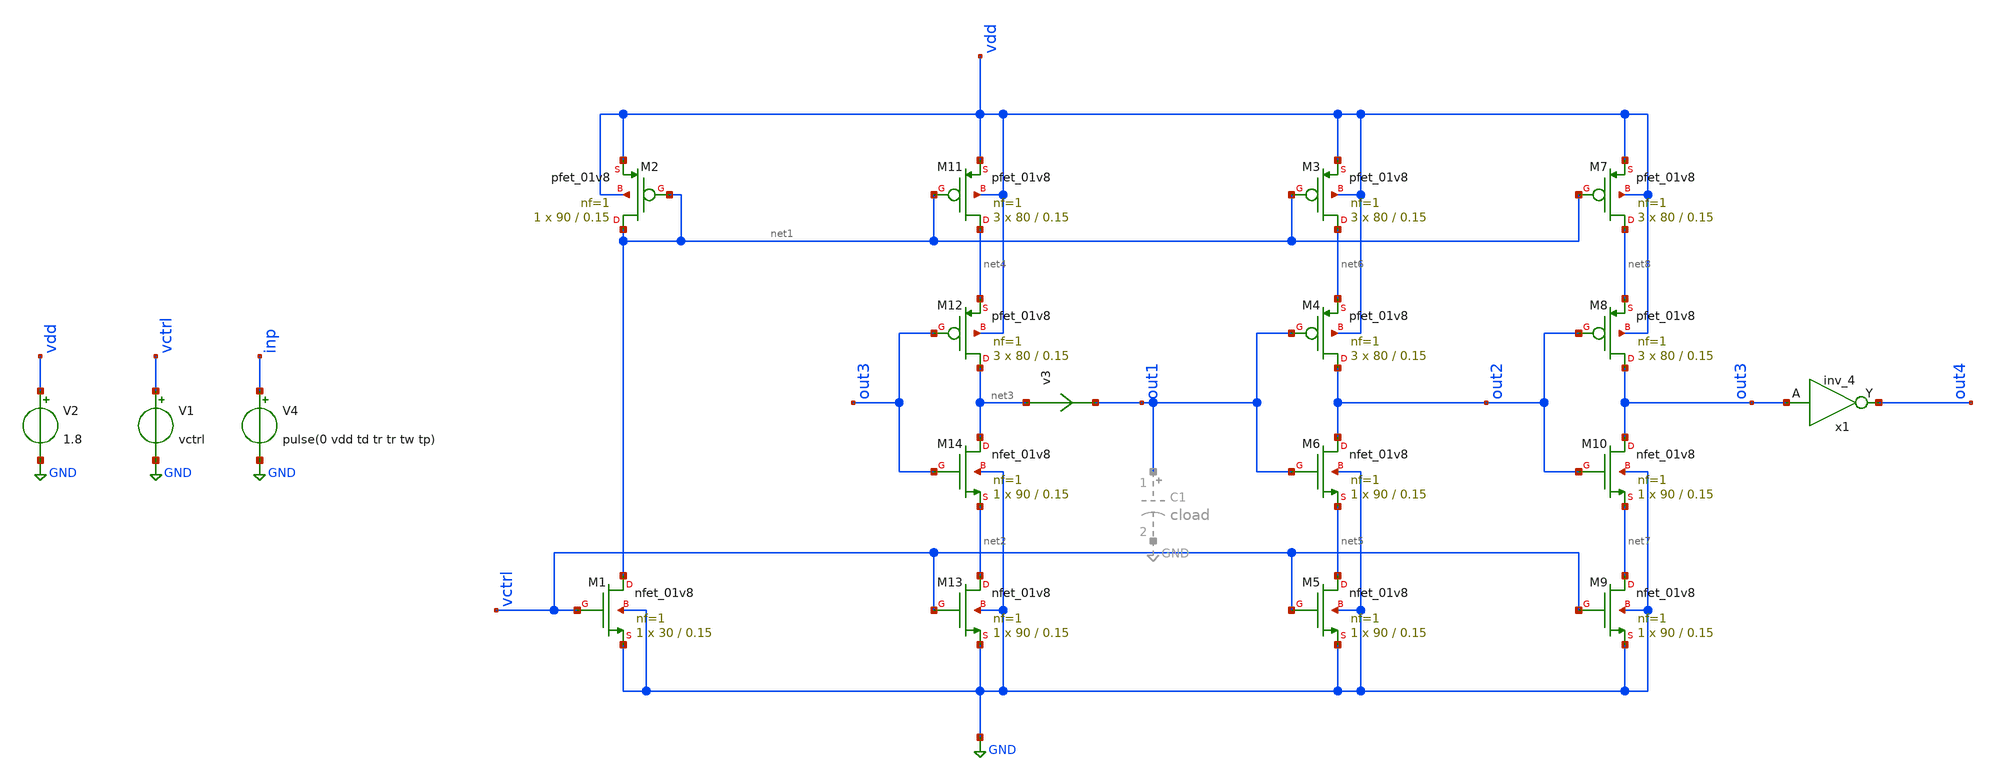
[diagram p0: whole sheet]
** sch_path: xschem/vco/inv_delay01_issue.sch
**.subckt inv_delay01_issue
XM1 net1 vctrl GND GND sky130_fd_pr__nfet_01v8 L=0.15 W=30 nf=1 ad='int((nf+1)/2) * W/nf * 0.29' as='int((nf+2)/2) * W/nf * 0.29'
+ pd='2*int((nf+1)/2) * (W/nf + 0.29)' ps='2*int((nf+2)/2) * (W/nf + 0.29)' nrd='0.29 / W' nrs='0.29 / W'
+ sa=0 sb=0 sd=0 mult=1 m=1
XM2 net1 net1 vdd vdd sky130_fd_pr__pfet_01v8 L=0.15 W=90 nf=1 ad='int((nf+1)/2) * W/nf * 0.29' as='int((nf+2)/2) * W/nf * 0.29'
+ pd='2*int((nf+1)/2) * (W/nf + 0.29)' ps='2*int((nf+2)/2) * (W/nf + 0.29)' nrd='0.29 / W' nrs='0.29 / W'
+ sa=0 sb=0 sd=0 mult=1 m=1
XM11 net4 net1 vdd vdd sky130_fd_pr__pfet_01v8 L=0.15 W=80 nf=1 ad='int((nf+1)/2) * W/nf * 0.29' as='int((nf+2)/2) * W/nf * 0.29'
+ pd='2*int((nf+1)/2) * (W/nf + 0.29)' ps='2*int((nf+2)/2) * (W/nf + 0.29)' nrd='0.29 / W' nrs='0.29 / W'
+ sa=0 sb=0 sd=0 mult=3 m=3
XM12 net3 out3 net4 vdd sky130_fd_pr__pfet_01v8 L=0.15 W=80 nf=1 ad='int((nf+1)/2) * W/nf * 0.29' as='int((nf+2)/2) * W/nf * 0.29'
+ pd='2*int((nf+1)/2) * (W/nf + 0.29)' ps='2*int((nf+2)/2) * (W/nf + 0.29)' nrd='0.29 / W' nrs='0.29 / W'
+ sa=0 sb=0 sd=0 mult=3 m=3
XM13 net2 vctrl GND GND sky130_fd_pr__nfet_01v8 L=0.15 W=90 nf=1 ad='int((nf+1)/2) * W/nf * 0.29' as='int((nf+2)/2) * W/nf * 0.29'
+ pd='2*int((nf+1)/2) * (W/nf + 0.29)' ps='2*int((nf+2)/2) * (W/nf + 0.29)' nrd='0.29 / W' nrs='0.29 / W'
+ sa=0 sb=0 sd=0 mult=1 m=1
XM14 net3 out3 net2 GND sky130_fd_pr__nfet_01v8 L=0.15 W=90 nf=1 ad='int((nf+1)/2) * W/nf * 0.29' as='int((nf+2)/2) * W/nf * 0.29'
+ pd='2*int((nf+1)/2) * (W/nf + 0.29)' ps='2*int((nf+2)/2) * (W/nf + 0.29)' nrd='0.29 / W' nrs='0.29 / W'
+ sa=0 sb=0 sd=0 mult=1 m=1
XM3 net6 net1 vdd vdd sky130_fd_pr__pfet_01v8 L=0.15 W=80 nf=1 ad='int((nf+1)/2) * W/nf * 0.29' as='int((nf+2)/2) * W/nf * 0.29'
+ pd='2*int((nf+1)/2) * (W/nf + 0.29)' ps='2*int((nf+2)/2) * (W/nf + 0.29)' nrd='0.29 / W' nrs='0.29 / W'
+ sa=0 sb=0 sd=0 mult=3 m=3
XM4 out2 out1 net6 vdd sky130_fd_pr__pfet_01v8 L=0.15 W=80 nf=1 ad='int((nf+1)/2) * W/nf * 0.29' as='int((nf+2)/2) * W/nf * 0.29'
+ pd='2*int((nf+1)/2) * (W/nf + 0.29)' ps='2*int((nf+2)/2) * (W/nf + 0.29)' nrd='0.29 / W' nrs='0.29 / W'
+ sa=0 sb=0 sd=0 mult=3 m=3
XM5 net5 vctrl GND GND sky130_fd_pr__nfet_01v8 L=0.15 W=90 nf=1 ad='int((nf+1)/2) * W/nf * 0.29' as='int((nf+2)/2) * W/nf * 0.29'
+ pd='2*int((nf+1)/2) * (W/nf + 0.29)' ps='2*int((nf+2)/2) * (W/nf + 0.29)' nrd='0.29 / W' nrs='0.29 / W'
+ sa=0 sb=0 sd=0 mult=1 m=1
XM6 out2 out1 net5 GND sky130_fd_pr__nfet_01v8 L=0.15 W=90 nf=1 ad='int((nf+1)/2) * W/nf * 0.29' as='int((nf+2)/2) * W/nf * 0.29'
+ pd='2*int((nf+1)/2) * (W/nf + 0.29)' ps='2*int((nf+2)/2) * (W/nf + 0.29)' nrd='0.29 / W' nrs='0.29 / W'
+ sa=0 sb=0 sd=0 mult=1 m=1
XM7 net8 net1 vdd vdd sky130_fd_pr__pfet_01v8 L=0.15 W=80 nf=1 ad='int((nf+1)/2) * W/nf * 0.29' as='int((nf+2)/2) * W/nf * 0.29'
+ pd='2*int((nf+1)/2) * (W/nf + 0.29)' ps='2*int((nf+2)/2) * (W/nf + 0.29)' nrd='0.29 / W' nrs='0.29 / W'
+ sa=0 sb=0 sd=0 mult=3 m=3
XM8 out3 out2 net8 vdd sky130_fd_pr__pfet_01v8 L=0.15 W=80 nf=1 ad='int((nf+1)/2) * W/nf * 0.29' as='int((nf+2)/2) * W/nf * 0.29'
+ pd='2*int((nf+1)/2) * (W/nf + 0.29)' ps='2*int((nf+2)/2) * (W/nf + 0.29)' nrd='0.29 / W' nrs='0.29 / W'
+ sa=0 sb=0 sd=0 mult=3 m=3
XM9 net7 vctrl GND GND sky130_fd_pr__nfet_01v8 L=0.15 W=90 nf=1 ad='int((nf+1)/2) * W/nf * 0.29' as='int((nf+2)/2) * W/nf * 0.29'
+ pd='2*int((nf+1)/2) * (W/nf + 0.29)' ps='2*int((nf+2)/2) * (W/nf + 0.29)' nrd='0.29 / W' nrs='0.29 / W'
+ sa=0 sb=0 sd=0 mult=1 m=1
XM10 out3 out2 net7 GND sky130_fd_pr__nfet_01v8 L=0.15 W=90 nf=1 ad='int((nf+1)/2) * W/nf * 0.29' as='int((nf+2)/2) * W/nf * 0.29'
+ pd='2*int((nf+1)/2) * (W/nf + 0.29)' ps='2*int((nf+2)/2) * (W/nf + 0.29)' nrd='0.29 / W' nrs='0.29 / W'
+ sa=0 sb=0 sd=0 mult=1 m=1
x1 out3 GND GND VDD VDD out4 sky130_fd_sc_hd__inv_4
v3 net3 out1 0
.save i(v3)
V1 vctrl GND vctrl
V2 vdd GND 1.8
V4 inp GND pulse(0 vdd td tr tr tw tp)
**** begin user architecture code

** opencircuitdesign pdks install
.lib $::SKYWATER_MODELS/sky130.lib.spice tt




.op
.options acct list
.temp 25

.include /usr/local/share/pdk/sky130A/libs.ref/sky130_fd_sc_hd/spice/sky130_fd_sc_hd.spice

.param vctrl=0.82 vdd=1.8 cload=250f  td=20n tr=0.1n tw=10n  tp=20n

.control
save all
save @m.xm1.msky130_fd_pr__nfet_01v8[cgd]
save @m.xm1.msky130_fd_pr__nfet_01v8[gm]

op
write inv_delay01.raw
set appendwrite

tran 0.001n 100n
meas tran tdelay01 TRIG v(out4) VAL=0.9 RISE=15 TARG v(out4) VAL=0.9 RISE=16
let fosc1= 1/tdelay01
print fosc1
save fosc1
remzerovec
write inv_delay01.raw


alterparam vctrl=0.83
reset
set appendwrite
tran 0.001n 100n
meas tran tdelay01 TRIG v(out4) VAL=0.9 RISE=15 TARG v(out4) VAL=0.9 RISE=16
let fosc1= 1/tdelay01
print fosc1
save fosc1
remzerovec
write inv_delay01.raw

.endc


**** end user architecture code
**.ends
.GLOBAL GND
.end
